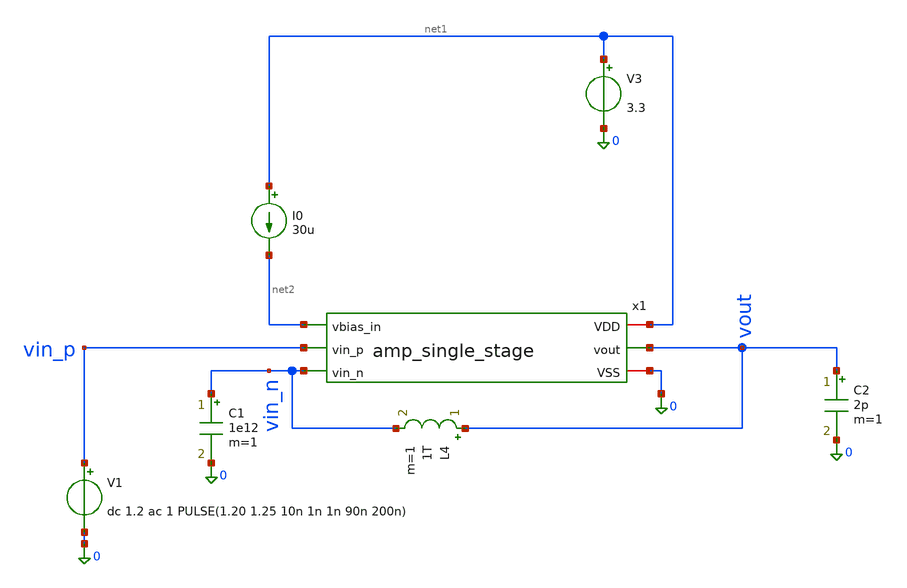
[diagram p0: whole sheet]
** sch_path: xschem/tb_amp_single_stg_ac.sch
**.subckt tb_amp_single_stg_ac
C2 vout 0 2p m=1
V3 net1 0 3.3
V1 vin_p 0 dc 1.2 ac 1 PULSE(1.20 1.25 10n 1n 1n 90n 200n)
L4 vout vin_n 1T m=1
C1 vin_n 0 1e12 m=1
x1 net1 net2 vout 0 vin_p vin_n amp_single_stage
I0 net1 net2 30u
**** begin user architecture code


* ======================================================================
* ADVANCED ANALOG OP-AMP TESTBENCH (GF180MCU)
* ======================================================================
* Process Corner Selection: typical, ff, ss, fs, sf
.param fnoicor = 0
.param sw_stat_global = 0
.param sw_stat_mismatch = 0

* PDK Model Include (MOSFETs)
.lib /foss/pdks/ciel/gf180mcu/versions/026824c7969ce6f4fc9678e6ca04b0a06a596c4b/gf180mcuD/libs.tech/ngspice/sm141064.ngspice typical

* MIM Capacitor Model (bypasses missing OSDI library)
.subckt cap_mim_2f0ff c0 c1 c_width=1e-6 c_length=1e-6
C_mim c0 c1 2.5p
.ends cap_mim_2f0ff

* Common-Mode AC Coupling Capacitor (1aF in diff mode, 1TF in CM mode)
C_cm vin_n vin_p 1e-18

* ======================================================================
* OPTIONAL: PEX EXTRACTION DUAL-DUT INSTANTIATION
* ======================================================================
* To compare ideal schematic vs layout extracted with Magic PEX:
* 1. Extract layout in Magic:
*    load tt_um_ece298_analog_op_amp; flatten tt_um_flat; load tt_um_flat
*    extract do local; extract all; ext2spice lvs; ext2spice cthresh 0.01; ext2spice -o
*+ /foss/designs/ttgf-ece298-analog-op-amp/mag/tt_um_flat_pex.spice
* 2. Uncomment the .include line below:
* .include /foss/designs/ttgf-ece298-analog-op-amp/mag/tt_um_flat_pex.spice
* 3. Uncomment the PEX instance and load cap below:
* XPEX 0 0 0 vin_p vin_n vout_pex net2 0 0 0 0 0 0 0 0 0 0 0 0 0 0 0 0 0 0 0 0 0 net1 tt_um_flat
* C2_pex vout_pex 0 2p

.save all

.control
destroy all
set color0=white
set color1=black
let pi = 3.141592653589793

* ======================================================================
* 1. DC OPERATING POINT & POWER
* ======================================================================
op

let v_inp_dc   = v(vin_p)
let v_inn_dc   = v(vin_n)
let v_out_dc   = v(vout)
let i_vdd_ua   = abs(v3#branch) * 1e6
let p_total_mw = i_vdd_ua * 3.3 / 1e3

echo ======================================================================
echo                    1. DC OPERATING POINT & POWER
echo ======================================================================
print v_inp_dc v_inn_dc v_out_dc
print i_vdd_ua p_total_mw

* ======================================================================
* 2. DIFFERENTIAL AC (GAIN, GBW, PM)
* ======================================================================
alter l4 = 1e12
alter c1 = 1e12
alter c_cm = 1e-18
alter v1 acmag = 1.0
alter v3 acmag = 0.0

ac dec 35 1 5G

let v_out_dm  = v(vout)
let gain_adm  = db(v_out_dm)
let phase_adm = cph(v_out_dm) * 180 / pi

meas ac a0_dm find gain_adm at=1
let g3db = a0_dm - 3
meas ac f3db when gain_adm = g3db
meas ac gbw when gain_adm = 0
meas ac ph_gbw find phase_adm when gain_adm = 0
let pm = 180 + ph_gbw

echo ======================================================================
echo                    2. DIFFERENTIAL AC RESULTS
echo ======================================================================
print a0_dm f3db gbw pm

plot gain_adm title 'Open-Loop Gain (dB)'
plot phase_adm title 'Open-Loop Phase (Deg)'

* ======================================================================
* 3. CMRR (COMMON-MODE REJECTION RATIO)
* ======================================================================
* For Common-Mode AC: open C1 and short vin_n to vin_p via C_cm
alter c1 = 1e-18
alter c_cm = 1e12
alter v1 acmag = 1.0

ac dec 35 1 5G

let v_out_cm = v(vout)
let gain_acm = db(v_out_cm)
let cmrr_vec = ac1.gain_adm - gain_acm

meas ac a0_cm find gain_acm at=1
meas ac cmrr_dc find cmrr_vec at=1
meas ac cmrr_10k find cmrr_vec at=10k
meas ac cmrr_1m find cmrr_vec at=1meg

echo ======================================================================
echo                    3. CMRR RESULTS
echo ======================================================================
print a0_cm cmrr_dc cmrr_10k cmrr_1m

* ======================================================================
* 4. PSRR+ (POWER SUPPLY REJECTION RATIO)
* ======================================================================
* Restore differential configuration, inject 1V AC onto VDD (v3)
alter c1 = 1e12
alter c_cm = 1e-18
alter v1 acmag = 0.0
alter v3 acmag = 1.0

ac dec 35 1 5G

let gain_supply = db(v(vout))
let psrr_vec = ac1.gain_adm - gain_supply

meas ac psrr_dc find psrr_vec at=1
meas ac psrr_10k find psrr_vec at=10k
meas ac psrr_1m find psrr_vec at=1meg

echo ======================================================================
echo                    4. PSRR+ RESULTS
echo ======================================================================
print psrr_dc psrr_10k psrr_1m

alter v3 acmag = 0.0

plot ac2.cmrr_vec ac3.psrr_vec title 'CMRR and PSRR+ vs Frequency (dB)'

* ======================================================================
* 5. MULTI-LINE LOAD CAPACITANCE SWEEP (CL = 0.5p, 1p, 2p, 5p)
* ======================================================================
alter v1 acmag = 1.0

alter c2 = 0.5p
ac dec 35 1 5G
alter c2 = 1.0p
ac dec 35 1 5G
alter c2 = 2.0p
ac dec 35 1 5G
alter c2 = 5.0p
ac dec 35 1 5G
alter c2 = 2p

plot db(ac4.v(vout)) db(ac5.v(vout)) db(ac6.v(vout)) db(ac7.v(vout)) title 'Gain vs CL: 0.5p (ac4), 1p (ac5), 2p (ac6), 5p (ac7)'
plot (cph(ac4.v(vout))*180/pi) (cph(ac5.v(vout))*180/pi) (cph(ac6.v(vout))*180/pi) (cph(ac7.v(vout))*180/pi)
+ title 'Phase vs CL: 0.5p, 1p, 2p, 5p'

* ======================================================================
* 6. MULTI-LINE BIAS CURRENT SWEEP (Iref = 20u, 25u, 30u, 35u)
* ======================================================================
alter i0 = 20u
ac dec 35 1 5G
alter i0 = 25u
ac dec 35 1 5G
alter i0 = 30u
ac dec 35 1 5G
alter i0 = 35u
ac dec 35 1 5G
alter i0 = 30u

plot db(ac8.v(vout)) db(ac9.v(vout)) db(ac10.v(vout)) db(ac11.v(vout)) title 'Gain vs Iref: 20u (ac8), 25u (ac9), 30u (ac10), 35u (ac11)'

* ======================================================================
* 7. TRANSIENT & SLEW RATE (CLOSED-LOOP UNITY-GAIN)
* ======================================================================
alter l4 = 1e-12
alter c1 = 1e-18
alter c_cm = 1e-18
alter v1 acmag = 0.0

tran 0.1n 1000n

meas tran t_rise TRIG v(vout) VAL=1.21 RISE=1 TARG v(vout) VAL=1.24 RISE=1 from=10n
meas tran t_fall TRIG v(vout) VAL=1.24 FALL=1 TARG v(vout) VAL=1.21 FALL=1 from=50n

let sr_rise_v_us = (0.03 / t_rise) / 1e6
let sr_fall_v_us = (0.03 / t_fall) / 1e6

echo ======================================================================
echo                    7. TRANSIENT & SLEW RATE RESULTS
echo ======================================================================
print sr_rise_v_us sr_fall_v_us

plot v(vout) v(vin_p) title 'Closed-Loop Transient Step Response'

* Ideal vs PEX Overlay (uncomment when PEX is enabled):
* plot db(ac1.v(vout)) db(ac1.v(vout_pex)) title 'Gain: Ideal vs PEX Extracted'

.endc


**** end user architecture code
**.ends

* expanding   symbol:  ttgf-ece298-analog-op-amp/xschem/amp_single_stage.sym # of pins=6
** sym_path: xschem/amp_single_stage.sym
** sch_path: xschem/amp_single_stage.sch
.subckt amp_single_stage VDD vbias_in vout VSS vin_p vin_n
*.opin vout
*.ipin vin_n
*.ipin vin_p
*.iopin VSS
*.iopin VDD
*.ipin vbias_in
x1 VDD vbias_in net1 net2 VSS amp_bias
x2 VDD vout net1 net2 vin_n vin_p vbias_in VSS amp_stg_1
.ends


* expanding   symbol:  ttgf-ece298-analog-op-amp/xschem/amp_bias.sym # of pins=5
** sym_path: xschem/amp_bias.sym
** sch_path: xschem/amp_bias.sch
.subckt amp_bias VDD vbias_in vbias_1 vbias_2 VSS
*.iopin VDD
*.iopin VSS
*.opin vbias_1
*.opin vbias_2
*.ipin vbias_in
XM1 vbias_in vbias_in VSS VSS nfet_03v3 L=1.4u W=32u nf=4 ad='int((nf+1)/2) * W/nf * 0.18u' as='int((nf+2)/2) * W/nf * 0.18u'
+ pd='2*int((nf+1)/2) * (W/nf + 0.18u)' ps='2*int((nf+2)/2) * (W/nf + 0.18u)' nrd='0.18u / W' nrs='0.18u / W'
+ sa=0 sb=0 sd=0 m=1 par=1
XM3 vbias_1 vbias_in VSS VSS nfet_03v3 L=1.4u W=8u nf=1 ad='int((nf+1)/2) * W/nf * 0.18u' as='int((nf+2)/2) * W/nf * 0.18u'
+ pd='2*int((nf+1)/2) * (W/nf + 0.18u)' ps='2*int((nf+2)/2) * (W/nf + 0.18u)' nrd='0.18u / W' nrs='0.18u / W'
+ sa=0 sb=0 sd=0 m=1 par=1
XM4 vbias_1 vbias_1 VDD VDD pfet_03v3 L=1.4u W=1u nf=1 ad='int((nf+1)/2) * W/nf * 0.18u' as='int((nf+2)/2) * W/nf * 0.18u'
+ pd='2*int((nf+1)/2) * (W/nf + 0.18u)' ps='2*int((nf+2)/2) * (W/nf + 0.18u)' nrd='0.18u / W' nrs='0.18u / W'
+ sa=0 sb=0 sd=0 m=1
XM5 vbias_2 vbias_1 VDD VDD pfet_03v3 L=1.4u W=1u nf=1 ad='int((nf+1)/2) * W/nf * 0.18u' as='int((nf+2)/2) * W/nf * 0.18u'
+ pd='2*int((nf+1)/2) * (W/nf + 0.18u)' ps='2*int((nf+2)/2) * (W/nf + 0.18u)' nrd='0.18u / W' nrs='0.18u / W'
+ sa=0 sb=0 sd=0 m=1
XM7 net1 vbias_2 VSS VSS nfet_03v3 L=9u W=1u nf=1 ad='int((nf+1)/2) * W/nf * 0.18u' as='int((nf+2)/2) * W/nf * 0.18u'
+ pd='2*int((nf+1)/2) * (W/nf + 0.18u)' ps='2*int((nf+2)/2) * (W/nf + 0.18u)' nrd='0.18u / W' nrs='0.18u / W'
+ sa=0 sb=0 sd=0 m=1 par=1
XM8 vbias_2 vbias_2 net1 VSS nfet_03v3 L=1.4u W=8u nf=1 ad='int((nf+1)/2) * W/nf * 0.18u' as='int((nf+2)/2) * W/nf * 0.18u'
+ pd='2*int((nf+1)/2) * (W/nf + 0.18u)' ps='2*int((nf+2)/2) * (W/nf + 0.18u)' nrd='0.18u / W' nrs='0.18u / W'
+ sa=0 sb=0 sd=0 m=1 par=1
.ends


* expanding   symbol:  ttgf-ece298-analog-op-amp/xschem/amp_stg_1.sym # of pins=8
** sym_path: xschem/amp_stg_1.sym
** sch_path: xschem/amp_stg_1.sch
.subckt amp_stg_1 VDD vout vbias_1 vbias_2 vn vp vbias_tail VSS
*.iopin VDD
*.iopin VSS
*.ipin vn
*.ipin vp
*.opin vout
*.ipin vbias_tail
*.ipin vbias_2
*.ipin vbias_1
XM2 net3 vbias_1 net1 VDD pfet_03v3 L=2.0u W=28u nf=4 ad='int((nf+1)/2) * W/nf * 0.18u' as='int((nf+2)/2) * W/nf * 0.18u'
+ pd='2*int((nf+1)/2) * (W/nf + 0.18u)' ps='2*int((nf+2)/2) * (W/nf + 0.18u)' nrd='0.18u / W' nrs='0.18u / W'
+ sa=0 sb=0 sd=0 m=1 par=1
XM1 net4 vn net6 VSS nfet_03v3 L=1.4u W=16u nf=2 ad='int((nf+1)/2) * W/nf * 0.18u' as='int((nf+2)/2) * W/nf * 0.18u'
+ pd='2*int((nf+1)/2) * (W/nf + 0.18u)' ps='2*int((nf+2)/2) * (W/nf + 0.18u)' nrd='0.18u / W' nrs='0.18u / W'
+ sa=0 sb=0 sd=0 m=2 par=2
XM3 net6 vbias_tail VSS VSS nfet_03v3 L=1.4u W=32u nf=4 ad='int((nf+1)/2) * W/nf * 0.18u' as='int((nf+2)/2) * W/nf * 0.18u'
+ pd='2*int((nf+1)/2) * (W/nf + 0.18u)' ps='2*int((nf+2)/2) * (W/nf + 0.18u)' nrd='0.18u / W' nrs='0.18u / W'
+ sa=0 sb=0 sd=0 m=1 par=1
XM4 vout vbias_2 net4 VSS nfet_03v3 L=2.0u W=16u nf=4 ad='int((nf+1)/2) * W/nf * 0.18u' as='int((nf+2)/2) * W/nf * 0.18u'
+ pd='2*int((nf+1)/2) * (W/nf + 0.18u)' ps='2*int((nf+2)/2) * (W/nf + 0.18u)' nrd='0.18u / W' nrs='0.18u / W'
+ sa=0 sb=0 sd=0 m=1 par=1
XM5 net3 vbias_2 net5 VSS nfet_03v3 L=2.0u W=16u nf=4 ad='int((nf+1)/2) * W/nf * 0.18u' as='int((nf+2)/2) * W/nf * 0.18u'
+ pd='2*int((nf+1)/2) * (W/nf + 0.18u)' ps='2*int((nf+2)/2) * (W/nf + 0.18u)' nrd='0.18u / W' nrs='0.18u / W'
+ sa=0 sb=0 sd=0 m=1 par=1
XM7 net5 vp net6 VSS nfet_03v3 L=1.4u W=16u nf=2 ad='int((nf+1)/2) * W/nf * 0.18u' as='int((nf+2)/2) * W/nf * 0.18u'
+ pd='2*int((nf+1)/2) * (W/nf + 0.18u)' ps='2*int((nf+2)/2) * (W/nf + 0.18u)' nrd='0.18u / W' nrs='0.18u / W'
+ sa=0 sb=0 sd=0 m=2 par=2
XM8 vout vbias_1 net2 VDD pfet_03v3 L=2.0u W=28u nf=4 ad='int((nf+1)/2) * W/nf * 0.18u' as='int((nf+2)/2) * W/nf * 0.18u'
+ pd='2*int((nf+1)/2) * (W/nf + 0.18u)' ps='2*int((nf+2)/2) * (W/nf + 0.18u)' nrd='0.18u / W' nrs='0.18u / W'
+ sa=0 sb=0 sd=0 m=1 par=1
XM9 net1 net3 VDD VDD pfet_03v3 L=2.0u W=28u nf=4 ad='int((nf+1)/2) * W/nf * 0.18u' as='int((nf+2)/2) * W/nf * 0.18u'
+ pd='2*int((nf+1)/2) * (W/nf + 0.18u)' ps='2*int((nf+2)/2) * (W/nf + 0.18u)' nrd='0.18u / W' nrs='0.18u / W'
+ sa=0 sb=0 sd=0 m=1 par=1
XM10 net2 net3 VDD VDD pfet_03v3 L=2.0u W=28u nf=4 ad='int((nf+1)/2) * W/nf * 0.18u' as='int((nf+2)/2) * W/nf * 0.18u'
+ pd='2*int((nf+1)/2) * (W/nf + 0.18u)' ps='2*int((nf+2)/2) * (W/nf + 0.18u)' nrd='0.18u / W' nrs='0.18u / W'
+ sa=0 sb=0 sd=0 m=1 par=1
XMD net6 VSS VSS VSS nfet_03v3 L=1.4u W=8u nf=1 ad='int((nf+1)/2) * W/nf * 0.18u' as='int((nf+2)/2) * W/nf * 0.18u'
+ pd='2*int((nf+1)/2) * (W/nf + 0.18u)' ps='2*int((nf+2)/2) * (W/nf + 0.18u)' nrd='0.18u / W' nrs='0.18u / W'
+ sa=0 sb=0 sd=0 m=2 par=2
.ends

.end
